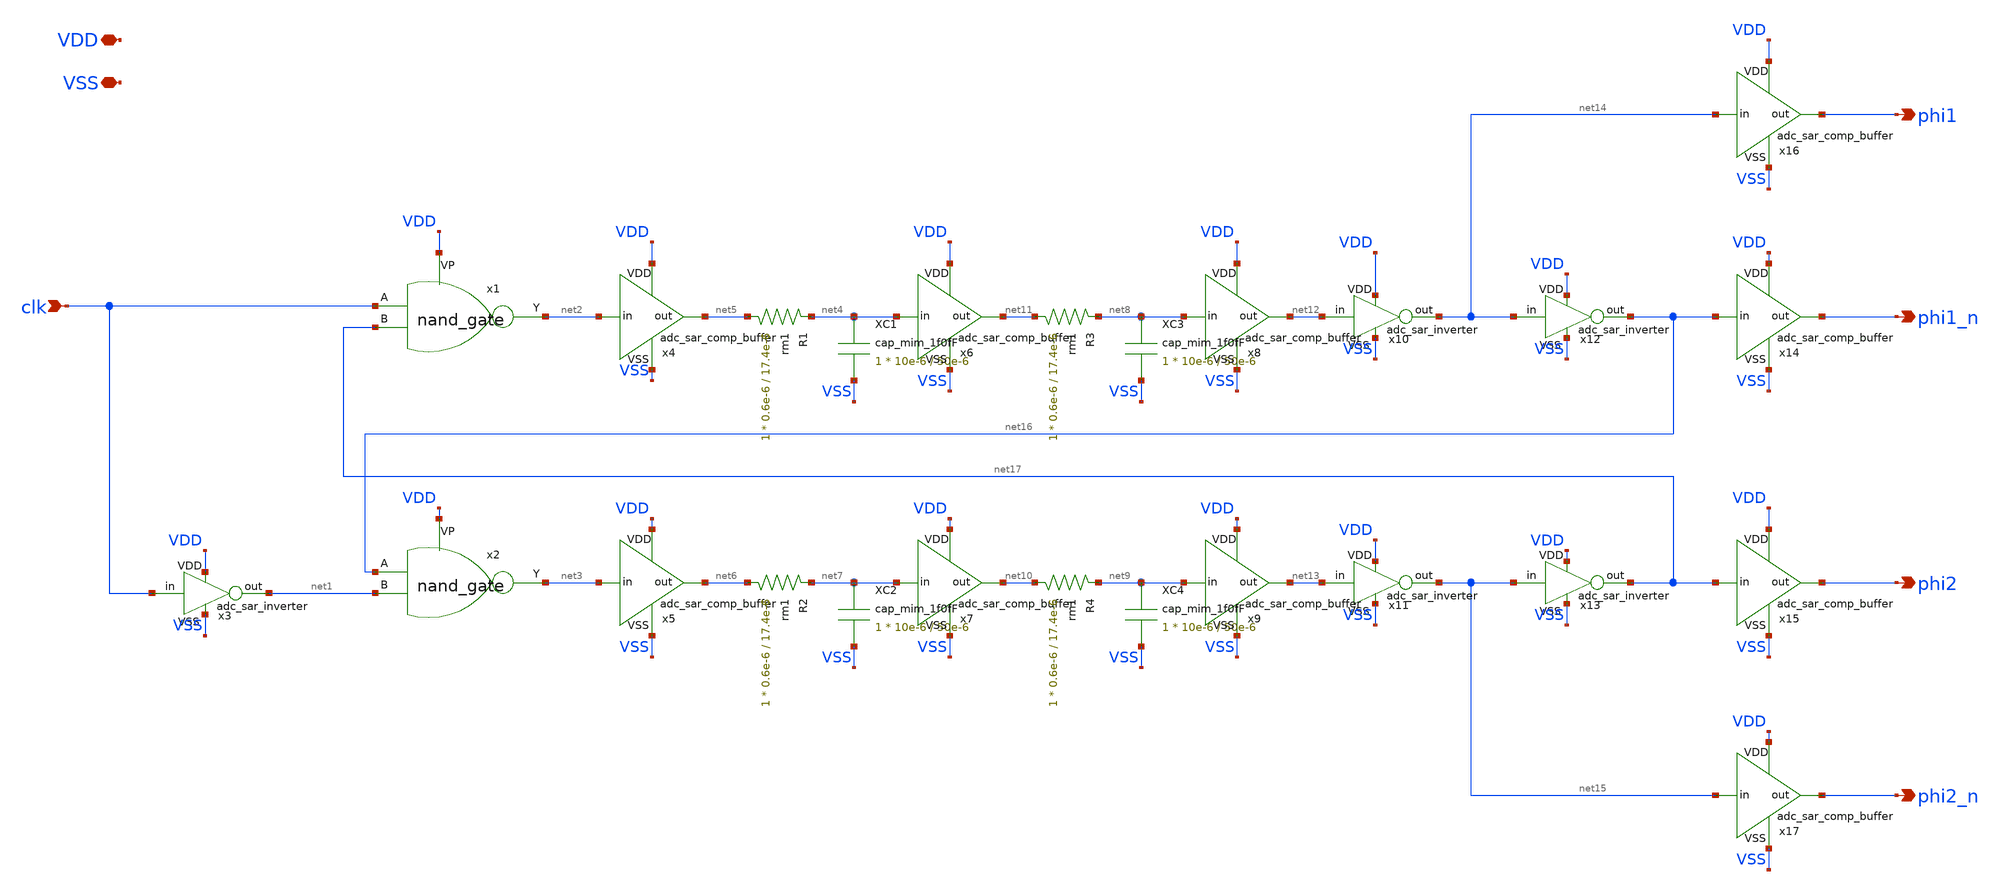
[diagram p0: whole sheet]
** sch_path: adc_sar_vcm_clk.sch
**.subckt adc_sar_vcm_clk VSS VDD clk phi1 phi1_n phi2 phi2_n
*.iopin VSS
*.iopin VDD
*.ipin clk
*.opin phi1
*.opin phi1_n
*.opin phi2
*.opin phi2_n
x1 VDD clk net17 net2 nand_gate
x2 VDD net16 net1 net3 nand_gate
x3 VDD VSS clk net1 adc_sar_inverter
x4 VDD VSS net2 net5 adc_sar_comp_buffer
x5 VDD VSS net3 net6 adc_sar_comp_buffer
XC1 net4 VSS cap_mim_1f0fF c_width=10e-6 c_length=50e-6 m=1
XR1 net5 net4 rm1 r_width=0.6e-6 r_length=17.4e-6 m=1
XC2 net7 VSS cap_mim_1f0fF c_width=10e-6 c_length=50e-6 m=1
XR2 net6 net7 rm1 r_width=0.6e-6 r_length=17.4e-6 m=1
x6 VDD VSS net4 net11 adc_sar_comp_buffer
x7 VDD VSS net7 net10 adc_sar_comp_buffer
XC3 net8 VSS cap_mim_1f0fF c_width=10e-6 c_length=50e-6 m=1
XR3 net11 net8 rm1 r_width=0.6e-6 r_length=17.4e-6 m=1
XC4 net9 VSS cap_mim_1f0fF c_width=10e-6 c_length=50e-6 m=1
XR4 net10 net9 rm1 r_width=0.6e-6 r_length=17.4e-6 m=1
x8 VDD VSS net8 net12 adc_sar_comp_buffer
x9 VDD VSS net9 net13 adc_sar_comp_buffer
x10 VDD VSS net12 net14 adc_sar_inverter
x11 VDD VSS net13 net15 adc_sar_inverter
x12 VDD VSS net14 net16 adc_sar_inverter
x13 VDD VSS net15 net17 adc_sar_inverter
x14 VDD VSS net16 phi1_n adc_sar_comp_buffer
x15 VDD VSS net17 phi2 adc_sar_comp_buffer
x16 VDD VSS net14 phi1 adc_sar_comp_buffer
x17 VDD VSS net15 phi2_n adc_sar_comp_buffer
**.ends

* expanding   symbol:  nand_gate.sym # of pins=4
** sym_path: nand_gate.sym
** sch_path: nand_gate.sch
.subckt nand_gate VP A B Y
*.ipin A
*.ipin B
*.opin Y
*.iopin VP
XM1 Y B net1 GND nfet_03v3 L=0.28u W=0.22u nf=1 ad='int((nf+1)/2) * W/nf * 0.18u' as='int((nf+2)/2) * W/nf * 0.18u'
+ pd='2*int((nf+1)/2) * (W/nf + 0.18u)' ps='2*int((nf+2)/2) * (W/nf + 0.18u)' nrd='0.18u / W' nrs='0.18u / W'
+ sa=0 sb=0 sd=0 m=1
XM2 Y A VP VP pfet_03v3 L=0.28u W=1u nf=1 ad='int((nf+1)/2) * W/nf * 0.18u' as='int((nf+2)/2) * W/nf * 0.18u'
+ pd='2*int((nf+1)/2) * (W/nf + 0.18u)' ps='2*int((nf+2)/2) * (W/nf + 0.18u)' nrd='0.18u / W' nrs='0.18u / W'
+ sa=0 sb=0 sd=0 m=1
XM4 net1 A GND GND nfet_03v3 L=0.28u W=0.22u nf=1 ad='int((nf+1)/2) * W/nf * 0.18u' as='int((nf+2)/2) * W/nf * 0.18u'
+ pd='2*int((nf+1)/2) * (W/nf + 0.18u)' ps='2*int((nf+2)/2) * (W/nf + 0.18u)' nrd='0.18u / W' nrs='0.18u / W'
+ sa=0 sb=0 sd=0 m=1
XM3 Y B VP VP pfet_03v3 L=0.28u W=1u nf=1 ad='int((nf+1)/2) * W/nf * 0.18u' as='int((nf+2)/2) * W/nf * 0.18u'
+ pd='2*int((nf+1)/2) * (W/nf + 0.18u)' ps='2*int((nf+2)/2) * (W/nf + 0.18u)' nrd='0.18u / W' nrs='0.18u / W'
+ sa=0 sb=0 sd=0 m=1
.ends


* expanding   symbol:  adc_sar_inverter.sym # of pins=4
** sym_path: adc_sar_inverter.sym
** sch_path: adc_sar_inverter.sch
.subckt adc_sar_inverter VDD VSS in out
*.iopin VDD
*.iopin VSS
*.ipin in
*.opin out
XM1 out in VSS VSS nfet_03v3 L=0.28u W=0.42u nf=1 ad='int((nf+1)/2) * W/nf * 0.18u' as='int((nf+2)/2) * W/nf * 0.18u'
+ pd='2*int((nf+1)/2) * (W/nf + 0.18u)' ps='2*int((nf+2)/2) * (W/nf + 0.18u)' nrd='0.18u / W' nrs='0.18u / W'
+ sa=0 sb=0 sd=0 m=1
XM2 out in VDD VDD pfet_03v3 L=0.28u W=0.84u nf=1 ad='int((nf+1)/2) * W/nf * 0.18u' as='int((nf+2)/2) * W/nf * 0.18u'
+ pd='2*int((nf+1)/2) * (W/nf + 0.18u)' ps='2*int((nf+2)/2) * (W/nf + 0.18u)' nrd='0.18u / W' nrs='0.18u / W'
+ sa=0 sb=0 sd=0 m=1
.ends


* expanding   symbol:  adc_sar_comp_buffer.sym # of pins=4
** sym_path: adc_sar_comp_buffer.sym
** sch_path: adc_sar_comp_buffer.sch
.subckt adc_sar_comp_buffer VDD VSS in out
*.iopin VDD
*.iopin VSS
*.ipin in
*.opin out
XM1 buf_mid in VSS VSS nfet_03v3 L=0.28u W=0.5u nf=1 ad='int((nf+1)/2) * W/nf * 0.18u' as='int((nf+2)/2) * W/nf * 0.18u'
+ pd='2*int((nf+1)/2) * (W/nf + 0.18u)' ps='2*int((nf+2)/2) * (W/nf + 0.18u)' nrd='0.18u / W' nrs='0.18u / W'
+ sa=0 sb=0 sd=0 m=1
XM2 out buf_mid VSS VSS nfet_03v3 L=0.28u W=1u nf=1 ad='int((nf+1)/2) * W/nf * 0.18u' as='int((nf+2)/2) * W/nf * 0.18u'
+ pd='2*int((nf+1)/2) * (W/nf + 0.18u)' ps='2*int((nf+2)/2) * (W/nf + 0.18u)' nrd='0.18u / W' nrs='0.18u / W'
+ sa=0 sb=0 sd=0 m=1
XM3 buf_mid in VDD VDD pfet_03v3 L=0.28u W=1u nf=1 ad='int((nf+1)/2) * W/nf * 0.18u' as='int((nf+2)/2) * W/nf * 0.18u'
+ pd='2*int((nf+1)/2) * (W/nf + 0.18u)' ps='2*int((nf+2)/2) * (W/nf + 0.18u)' nrd='0.18u / W' nrs='0.18u / W'
+ sa=0 sb=0 sd=0 m=1
XM4 out buf_mid VDD VDD pfet_03v3 L=0.28u W=2u nf=1 ad='int((nf+1)/2) * W/nf * 0.18u' as='int((nf+2)/2) * W/nf * 0.18u'
+ pd='2*int((nf+1)/2) * (W/nf + 0.18u)' ps='2*int((nf+2)/2) * (W/nf + 0.18u)' nrd='0.18u / W' nrs='0.18u / W'
+ sa=0 sb=0 sd=0 m=1
.ends

.GLOBAL GND
.end
